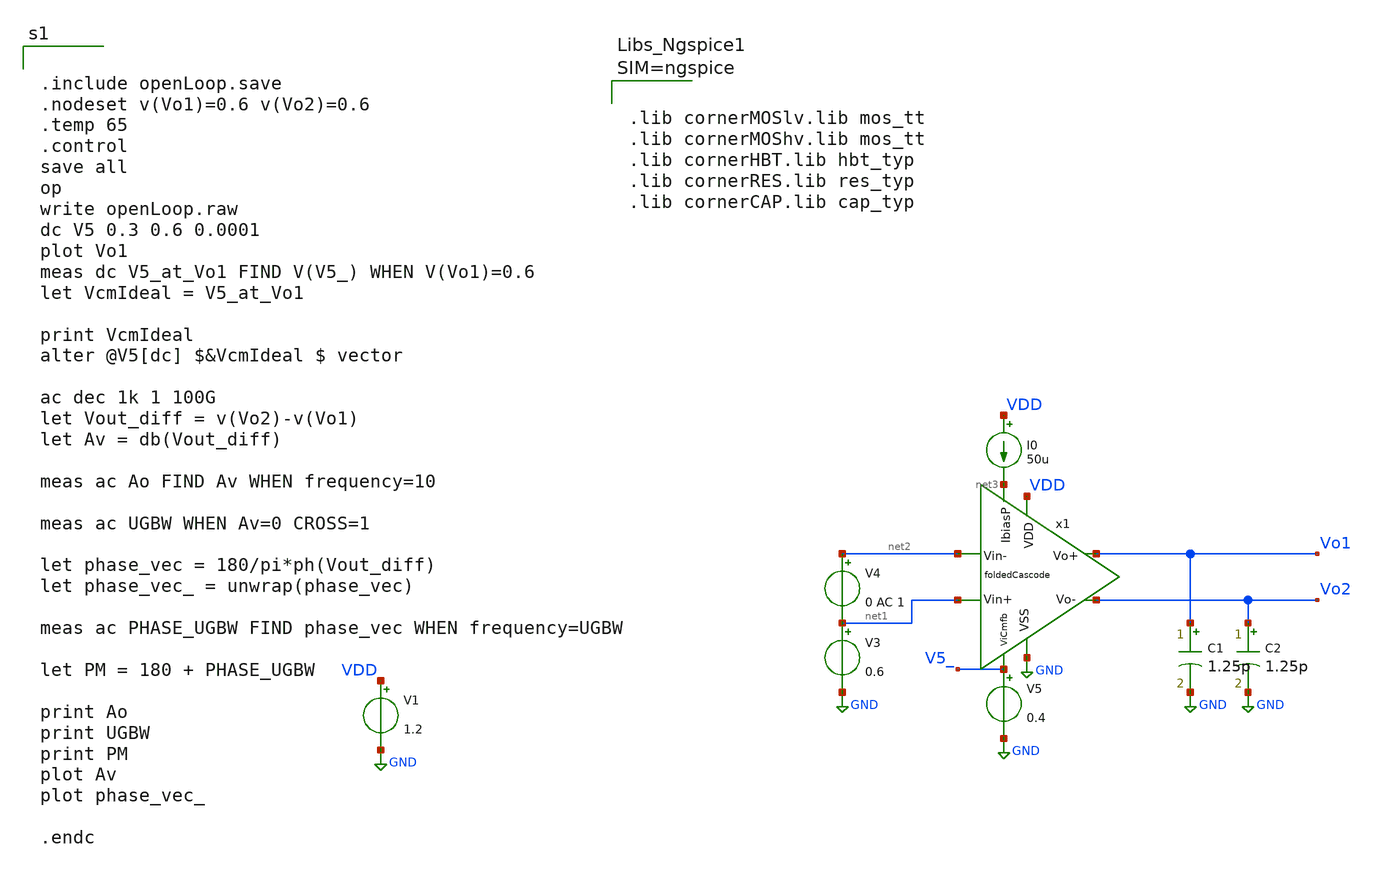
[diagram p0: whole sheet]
** sch_path: sch/tb/openLoop.sch
**.subckt openLoop
x1 VDD GND V5_ net3 Vo1 Vo2 net2 net1 foldedCascode
V1 VDD GND 1.2
V3 net1 GND 0.6
V4 net2 net1 0 AC 1
C1 Vo1 GND 1.25p m=1
C2 Vo2 GND 1.25p m=1
V5 V5_ GND 0.4
I0 VDD net3 50u
**** begin user architecture code


.include openLoop.save
.nodeset v(Vo1)=0.6 v(Vo2)=0.6
.temp 65
.control
save all
op
write openLoop.raw
dc V5 0.3 0.6 0.0001
plot Vo1
meas dc V5_at_Vo1 FIND V(V5_) WHEN V(Vo1)=0.6
let VcmIdeal = V5_at_Vo1

print VcmIdeal
alter @V5[dc] $&VcmIdeal $ vector

ac dec 1k 1 100G
let Vout_diff = v(Vo2)-v(Vo1)
let Av = db(Vout_diff)

meas ac Ao FIND Av WHEN frequency=10

meas ac UGBW WHEN Av=0 CROSS=1

let phase_vec = 180/pi*ph(Vout_diff)
let phase_vec_ = unwrap(phase_vec)

meas ac PHASE_UGBW FIND phase_vec WHEN frequency=UGBW

let PM = 180 + PHASE_UGBW

print Ao
print UGBW
print PM
plot Av
plot phase_vec_

.endc





.lib cornerMOSlv.lib mos_tt
.lib cornerMOShv.lib mos_tt
.lib cornerHBT.lib hbt_typ
.lib cornerRES.lib res_typ
.lib cornerCAP.lib cap_typ



**** end user architecture code
**.ends

* expanding   symbol:  foldedCascode.sym # of pins=8
** sym_path: sch/blocks/foldedCascode.sym
** sch_path: sch/blocks/foldedCascode.sch
.subckt foldedCascode VDD VSS ViCmfb IbiasP Vo+ Vo- Vin- Vin+
*.iopin VSS
*.iopin VDD
*.ipin ViCmfb
*.iopin IbiasP
*.ipin Vin+
*.ipin Vin-
*.iopin Vo+
*.iopin Vo-
x1 VDD Vb1_1 Vb1_2 Vx Vy VSS IbiasN gmBoosting
XM1 Vy Vin+ net3 net3 sg13_lv_pmos w=115u l=0.13u ng=100 m=2 mm_ok=1
XM2 Vx Vin- net3 net3 sg13_lv_pmos w=115u l=0.13u ng=100 m=2 mm_ok=1
XM3 Vo+ Vb1_1 Vx VSS sg13_lv_nmos w=44.4u l=0.3u ng=22 m=6 mm_ok=1
XM12 Vx ViCmfb VSS VSS sg13_lv_nmos w=24.3u l=0.8u ng=62 m=6 mm_ok=1
XM4 Vo- Vb1_2 Vy VSS sg13_lv_nmos w=44.4u l=0.3u ng=22 m=6 mm_ok=1
XM5 Vy ViCmfb VSS VSS sg13_lv_nmos w=24.3u l=0.8u ng=62 m=6 mm_ok=1
XM6 Vb0 Vb0 net4 VDD sg13_lv_pmos w=65u l=0.13u ng=65 m=1 mm_ok=1
XM13 net4 Vb0 VDD VDD sg13_lv_pmos w=26u l=0.3u ng=5 m=1 mm_ok=1
XM20 Vb3 Vb2 net6 VDD sg13_lv_pmos w=5.6u l=0.4u ng=1 m=1 mm_ok=1
XM21 net6 Vb3 VDD VDD sg13_lv_pmos w=9.7u l=0.8u ng=2 m=1 mm_ok=1
XM14 IbiasP IbiasP VSS VSS sg13_lv_nmos w=2u l=1u ng=2 m=10 mm_ok=1
XM11 Vb0 IbiasP VSS VSS sg13_lv_nmos w=2u l=1u ng=2 m=2 mm_ok=1
XM15 Vb3 IbiasP VSS VSS sg13_lv_nmos w=2u l=1u ng=2 m=2 mm_ok=1
XM16 Vb2 IbiasP VSS VSS sg13_lv_nmos w=2u l=1u ng=2 m=5 mm_ok=1
XM22 IbiasN IbiasP VSS VSS sg13_lv_nmos w=1.8u l=1u ng=2 m=10 mm_ok=1
XM23 net1 Vb3 VDD VDD sg13_lv_pmos w=63.2u l=0.8u ng=103 m=4 mm_ok=1
XM9 net2 Vb3 VDD VDD sg13_lv_pmos w=63.2u l=0.8u ng=103 m=4 mm_ok=1
XM10 Vo+ Vb2 net1 VDD sg13_lv_pmos w=100u l=0.4u ng=150 m=4 mm_ok=1
XM7 Vo- Vb2 net2 VDD sg13_lv_pmos w=100u l=0.4u ng=150 m=4 mm_ok=1
XM8 net5 Vb2 VDD VDD sg13_lv_pmos w=5.8u l=0.7u ng=1 m=1 mm_ok=1
XM17 Vb2 Vb2 net5 VDD sg13_lv_pmos w=27u l=0.4u ng=9 m=1 mm_ok=1
XM0 net3 Vb0 VDD VDD sg13_lv_pmos w=113.5u l=0.3u ng=210 m=8 mm_ok=1
.ends


* expanding   symbol:  gmBoosting.sym # of pins=7
** sym_path: sch/blocks/gmBoosting.sym
** sch_path: sch/blocks/gmBoosting.sch
.subckt gmBoosting VDD Vo2 Vo1 Vi+ Vi- VSS IbiasN
*.iopin VSS
*.opin Vo1
*.opin Vo2
*.ipin Vi+
*.ipin Vi-
*.iopin VDD
*.ipin IbiasN
XM7 net2 Vb4 VDD VDD sg13_lv_pmos w=19.8u l=0.7u ng=20 m=2 mm_ok=1
XM1 net7 Vi+ net1 net1 sg13_lv_pmos w=35u l=0.15u ng=70 m=4 mm_ok=1
XM2 net4 Vi- net1 net1 sg13_lv_pmos w=35u l=0.15u ng=70 m=4 mm_ok=1
XM0 net1 Vb0 net5 VDD sg13_lv_pmos w=12u l=0.3u ng=12 m=1 mm_ok=1
XM6 net7 Vb3 VSS VSS sg13_lv_nmos w=20.2u l=0.7u ng=5 m=2 mm_ok=1
XM9 Vo1 Vb2 net2 VDD sg13_lv_pmos w=23.2u l=0.3u ng=10 m=1 mm_ok=1
XM10 Vo2 Vb2 net3 VDD sg13_lv_pmos w=23.2u l=0.3u ng=10 m=1 mm_ok=1
XM3 net5 Vo2 VDD VDD sg13_lv_pmos w=20u l=0.13u ng=5 m=1 mm_ok=1
XM4 net5 Vo1 VDD VDD sg13_lv_pmos w=20u l=0.13u ng=5 m=1 mm_ok=1
XM5 net6 Va VDD VDD sg13_lv_pmos w=20u l=0.13u ng=5 m=2 mm_ok=1
XM29 Vb3 Vb3 VSS VSS sg13_lv_nmos w=32u l=0.7u ng=4 m=1 mm_ok=1
XM30 Vb3 Vb0 net6 VDD sg13_lv_pmos w=12u l=0.3u ng=12 m=1 mm_ok=1
XM31 net4 Vb3 VSS VSS sg13_lv_nmos w=20.2u l=0.7u ng=5 m=2 mm_ok=1
XM32 Vo1 Vb1 net4 VSS sg13_lv_nmos w=38.7u l=0.6u ng=5 m=1 mm_ok=1
XM21 IbiasN IbiasN VDD VDD sg13_lv_pmos w=18u l=1u ng=18 m=1 mm_ok=1
XM24 VbbN IbiasN VDD VDD sg13_lv_pmos w=18u l=1u ng=18 m=1 mm_ok=1
XM25 VbbN VbbN VSS VSS sg13_lv_nmos w=15u l=1u ng=2 m=1 mm_ok=1
XM17 Va VbbN VSS VSS sg13_lv_nmos w=15u l=1u ng=2 m=1 mm_ok=1
XM18 Va Va VDD VDD sg13_lv_pmos w=13u l=1u ng=13 m=1 mm_ok=1
XM19 Vb1 Vb1 net9 VSS sg13_lv_nmos w=13u l=0.7u ng=2 m=1 mm_ok=1
XM20 net9 Vb1 VSS VSS sg13_lv_nmos w=2.4u l=0.7u ng=1 m=1 mm_ok=1
XM22 Vb1 IbiasN VDD VDD sg13_lv_pmos w=18u l=1u ng=18 m=1 mm_ok=1
XM26 Vb4 Vb2 net8 VDD sg13_lv_pmos w=9u l=0.3u ng=9 m=1 mm_ok=1
XM38 net8 Vb4 VDD VDD sg13_lv_pmos w=15.5u l=0.7u ng=15 m=1 mm_ok=1
XM39 Vb4 VbbN VSS VSS sg13_lv_nmos w=15u l=1u ng=2 m=1 mm_ok=1
XM40 net11 Vb2 VDD VDD sg13_lv_pmos w=4.5u l=0.7u ng=1 m=1 mm_ok=1
XM41 Vb2 Vb2 net11 VDD sg13_lv_pmos w=15u l=0.7u ng=15 m=1 mm_ok=1
XM42 Vb2 VbbN VSS VSS sg13_lv_nmos w=15u l=1u ng=2 m=1 mm_ok=1
XM8 net3 Vb4 VDD VDD sg13_lv_pmos w=19.8u l=0.7u ng=20 m=2 mm_ok=1
XM11 Vo2 Vb1 net7 VSS sg13_lv_nmos w=38.7u l=0.6u ng=5 m=1 mm_ok=1
XM12 Vb0 VbbN VSS VSS sg13_lv_nmos w=15u l=1u ng=2 m=1 mm_ok=1
XM13 net10 Vb0 VDD VDD sg13_lv_pmos w=3.92u l=0.7u ng=2 m=1 mm_ok=1
XM14 Vb0 Vb0 net10 VDD sg13_lv_pmos w=55u l=0.15u ng=55 m=1 mm_ok=1
.ends

.GLOBAL GND
.end
